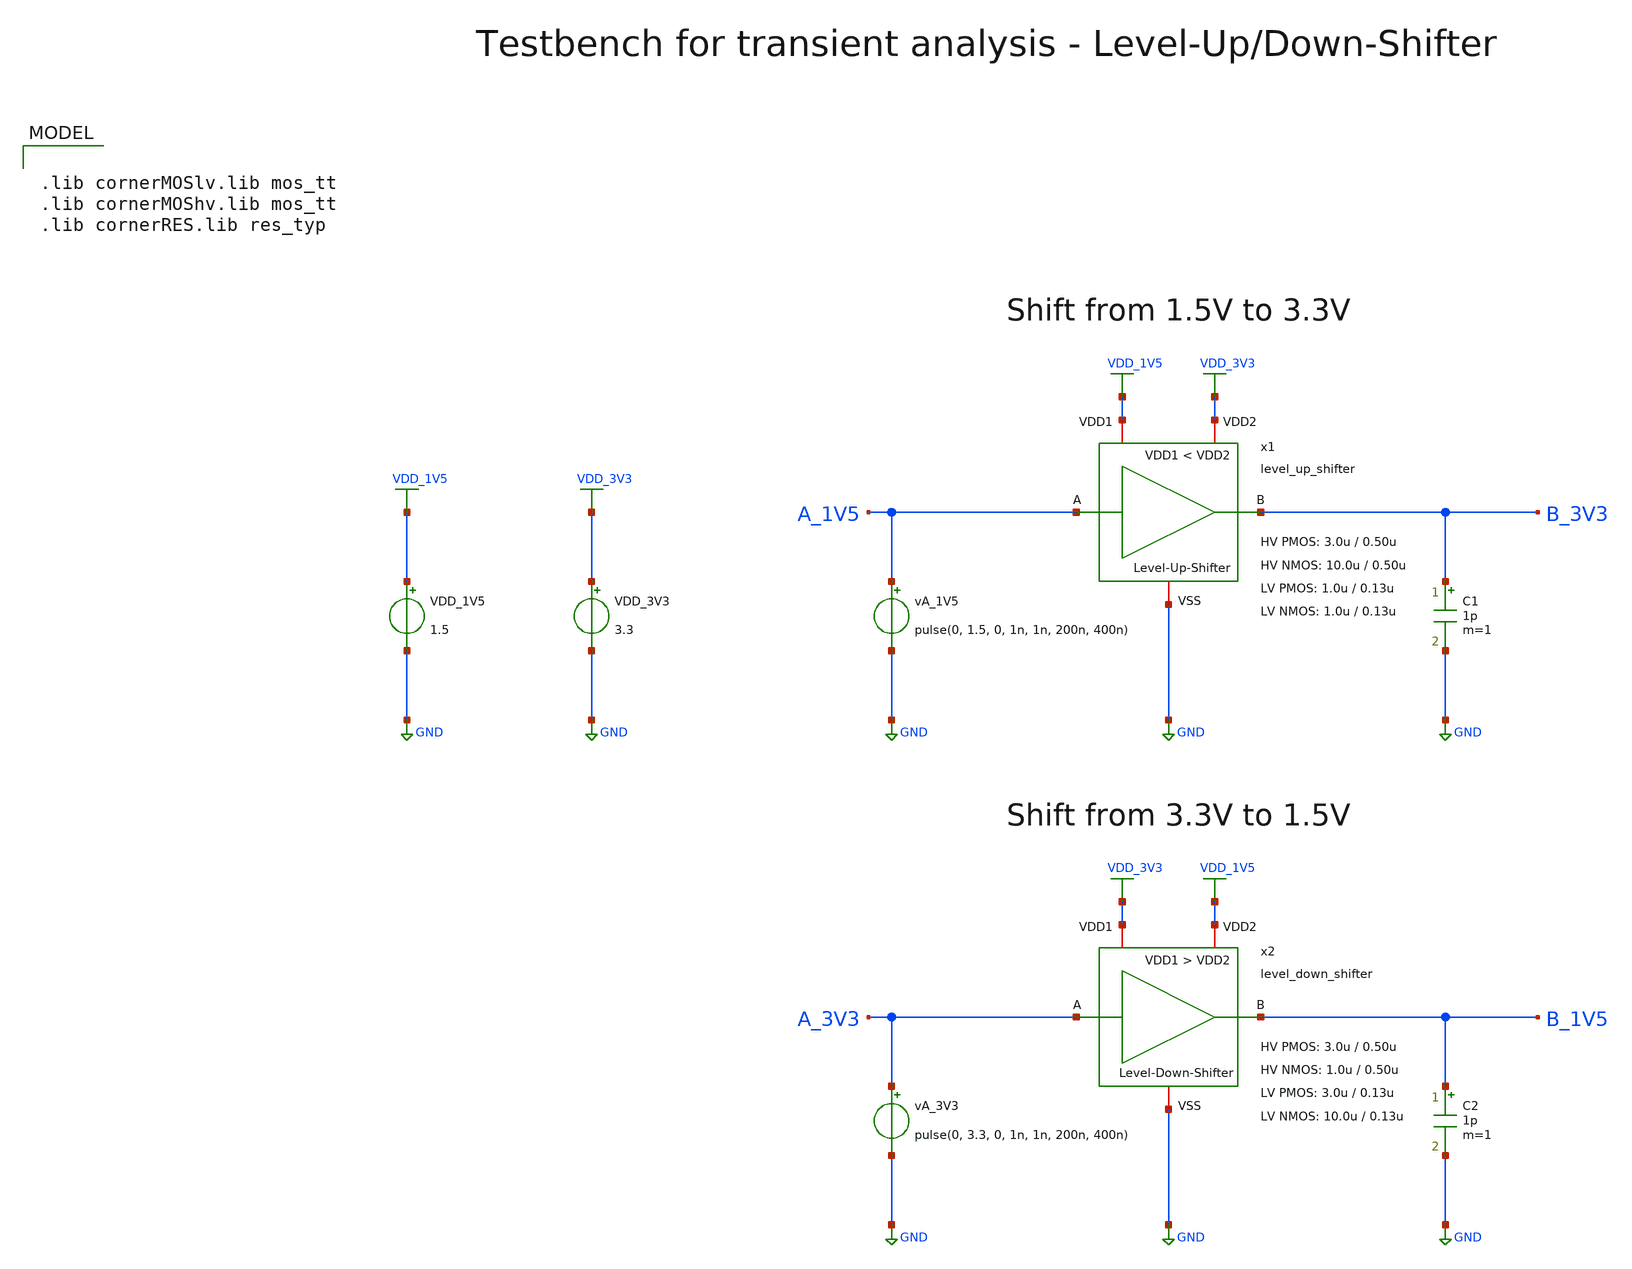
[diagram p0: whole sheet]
** sch_path: SG13G2_ATBS-ADC-main/xschem/level_shifter/testbenches/level_shifter_tb_tran.sch
**.subckt level_shifter_tb_tran
VDD_1V5 VDD_1V5 GND 1.5
vA_1V5 A_1V5 GND pulse(0, 1.5, 0, 1n, 1n, 200n, 400n)
C1 B_3V3 GND 1p m=1
VDD_3V3 VDD_3V3 GND 3.3
vA_3V3 A_3V3 GND pulse(0, 3.3, 0, 1n, 1n, 200n, 400n)
C2 B_1V5 GND 1p m=1
x1 VDD_3V3 A_1V5 B_3V3 GND VDD_1V5 level_up_shifter W_P_HV=3.0u L_P_HV=0.50u W_N_HV=10.0u
+ L_N_HV=0.50u W_P_LV=1.0u L_P_LV=0.13u W_N_LV=1.0u L_N_LV=0.13u
x2 VDD_1V5 A_3V3 B_1V5 GND VDD_3V3 level_down_shifter W_P_HV=3.0u L_P_HV=0.50u W_N_HV=1.0u
+ L_N_HV=0.50u W_P_LV=3.0u L_P_LV=0.13u W_N_LV=10.0u L_N_LV=0.13u
**** begin user architecture code

.lib cornerMOSlv.lib mos_tt
.lib cornerMOShv.lib mos_tt
.lib cornerRES.lib res_typ



.param temp=27
.options savecurrents
.control
save all

* Operating Point Analysis
op
remzerovec
write level_shifter_tb_tran.raw
set appendwrite

* Transient Analysis
tran 100p 400n
write level_shifter_tb_tran.raw

* Writing Data
set wr_singlescale
set wr_vecnames
let x1t = x1.t
let x2t = x2.t
wrdata /foss/designs/SG13G2_ATBS-ADC-main/python/plot_simulations/data/level_shifter_tb_tran.txt
+ v(a_1V5) v(b_3V3) v(x1t) v(a_3V3) v(b_1V5) v(x2t)

quit
.endc


**** end user architecture code
**.ends

* expanding   symbol:  level_shifter/level_up_shifter.sym # of pins=5
** sym_path: SG13G2_ATBS-ADC-main/xschem/level_shifter/level_up_shifter.sym
** sch_path: SG13G2_ATBS-ADC-main/xschem/level_shifter/level_up_shifter.sch
.subckt level_up_shifter VDD2 A B VSS VDD1  W_P_HV=3.0u L_P_HV=0.50u W_N_HV=10.0u L_N_HV=0.50u
+ W_P_LV=1.0u L_P_LV=0.13u W_N_LV=1.0u L_N_LV=0.13u
*.ipin A
*.iopin VDD1
*.iopin VSS
*.opin B
*.iopin VDD2
x1 VDD1 A A! VSS inverter_lv W_P=W_P_LV L_P=L_P_LV W_N=W_N_LV L_N=L_N_LV
XM1 net1 A! VSS VSS sg13_hv_nmos w=W_N_HV l=L_N_HV ng=1 m=1 mm_ok=1
XM4 T net1 VDD2 VDD2 sg13_hv_pmos w=W_P_HV l=L_P_HV ng=1 m=1 mm_ok=1
x2 VDD1 A! net2 VSS inverter_lv W_P=W_P_LV L_P=L_P_LV W_N=W_N_LV L_N=L_N_LV
XM3 net1 T VDD2 VDD2 sg13_hv_pmos w=W_P_HV l=L_P_HV ng=1 m=1 mm_ok=1
XM2 T net2 VSS VSS sg13_hv_nmos w=W_N_HV l=L_N_HV ng=1 m=1 mm_ok=1
x3 VDD2 T B VSS inverter_hv W_P=W_P_HV L_P=L_P_HV W_N=0.1*W_N_HV L_N=L_N_HV
.ends


* expanding   symbol:  level_shifter/level_down_shifter.sym # of pins=5
** sym_path: SG13G2_ATBS-ADC-main/xschem/level_shifter/level_down_shifter.sym
** sch_path: SG13G2_ATBS-ADC-main/xschem/level_shifter/level_down_shifter.sch
.subckt level_down_shifter VDD2 A B VSS VDD1  W_P_HV=3.0u L_P_HV=0.50u W_N_HV=1.0u L_N_HV=0.50u
+ W_P_LV=3.0u L_P_LV=0.13u W_N_LV=10.0u L_N_LV=0.13u
*.ipin A
*.iopin VDD1
*.iopin VSS
*.opin B
*.iopin VDD2
x3 VDD2 T B VSS inverter_lv W_P=W_P_LV L_P=L_P_LV W_N=0.1*W_N_LV L_N=L_N_LV
x1 VDD1 A A! VSS inverter_hv W_P=W_P_HV L_P=L_P_HV W_N=W_N_HV L_N=L_N_HV
x2 VDD1 A! net2 VSS inverter_hv W_P=W_P_HV L_P=L_P_HV W_N=W_N_HV L_N=L_N_HV
XM1 net1 A! VSS VSS sg13_lv_nmos w=W_N_LV l=L_N_LV ng=1 m=1 mm_ok=1
XM3 net1 T VDD2 VDD2 sg13_lv_pmos w=W_P_LV l=L_P_LV ng=1 m=1 mm_ok=1
XM2 T net2 VSS VSS sg13_lv_nmos w=W_N_LV l=L_N_LV ng=1 m=1 mm_ok=1
XM4 T net1 VDD2 VDD2 sg13_lv_pmos w=W_P_LV l=L_P_LV ng=1 m=1 mm_ok=1
.ends


* expanding   symbol:  inverter/inverter_lv.sym # of pins=4
** sym_path: SG13G2_ATBS-ADC-main/xschem/inverter/inverter_lv.sym
** sch_path: SG13G2_ATBS-ADC-main/xschem/inverter/inverter_lv.sch
.subckt inverter_lv VDD vin vout VSS  W_P=3.0u L_P=0.13u W_N=1.0u L_N=0.13u
*.ipin vin
*.iopin VDD
*.iopin VSS
*.opin vout
XM1 vout vin VDD VDD sg13_lv_pmos w=W_P l=L_P ng=1 m=1 mm_ok=1
XM2 vout vin VSS VSS sg13_lv_nmos w=W_N l=L_N ng=1 m=1 mm_ok=1
.ends


* expanding   symbol:  inverter/inverter_hv.sym # of pins=4
** sym_path: SG13G2_ATBS-ADC-main/xschem/inverter/inverter_hv.sym
** sch_path: SG13G2_ATBS-ADC-main/xschem/inverter/inverter_hv.sch
.subckt inverter_hv VDD vin vout VSS  W_P=3.0u L_P=0.50u W_N=1.0u L_N=0.50u
*.ipin vin
*.iopin VDD
*.iopin VSS
*.opin vout
XM1 vout vin VDD VDD sg13_hv_pmos w=W_P l=L_P ng=1 m=1 mm_ok=1
XM2 vout vin VSS VSS sg13_hv_nmos w=W_N l=L_N ng=1 m=1 mm_ok=1
.ends

.GLOBAL GND
.GLOBAL VDD_1V5
.GLOBAL VDD_3V3
.end
